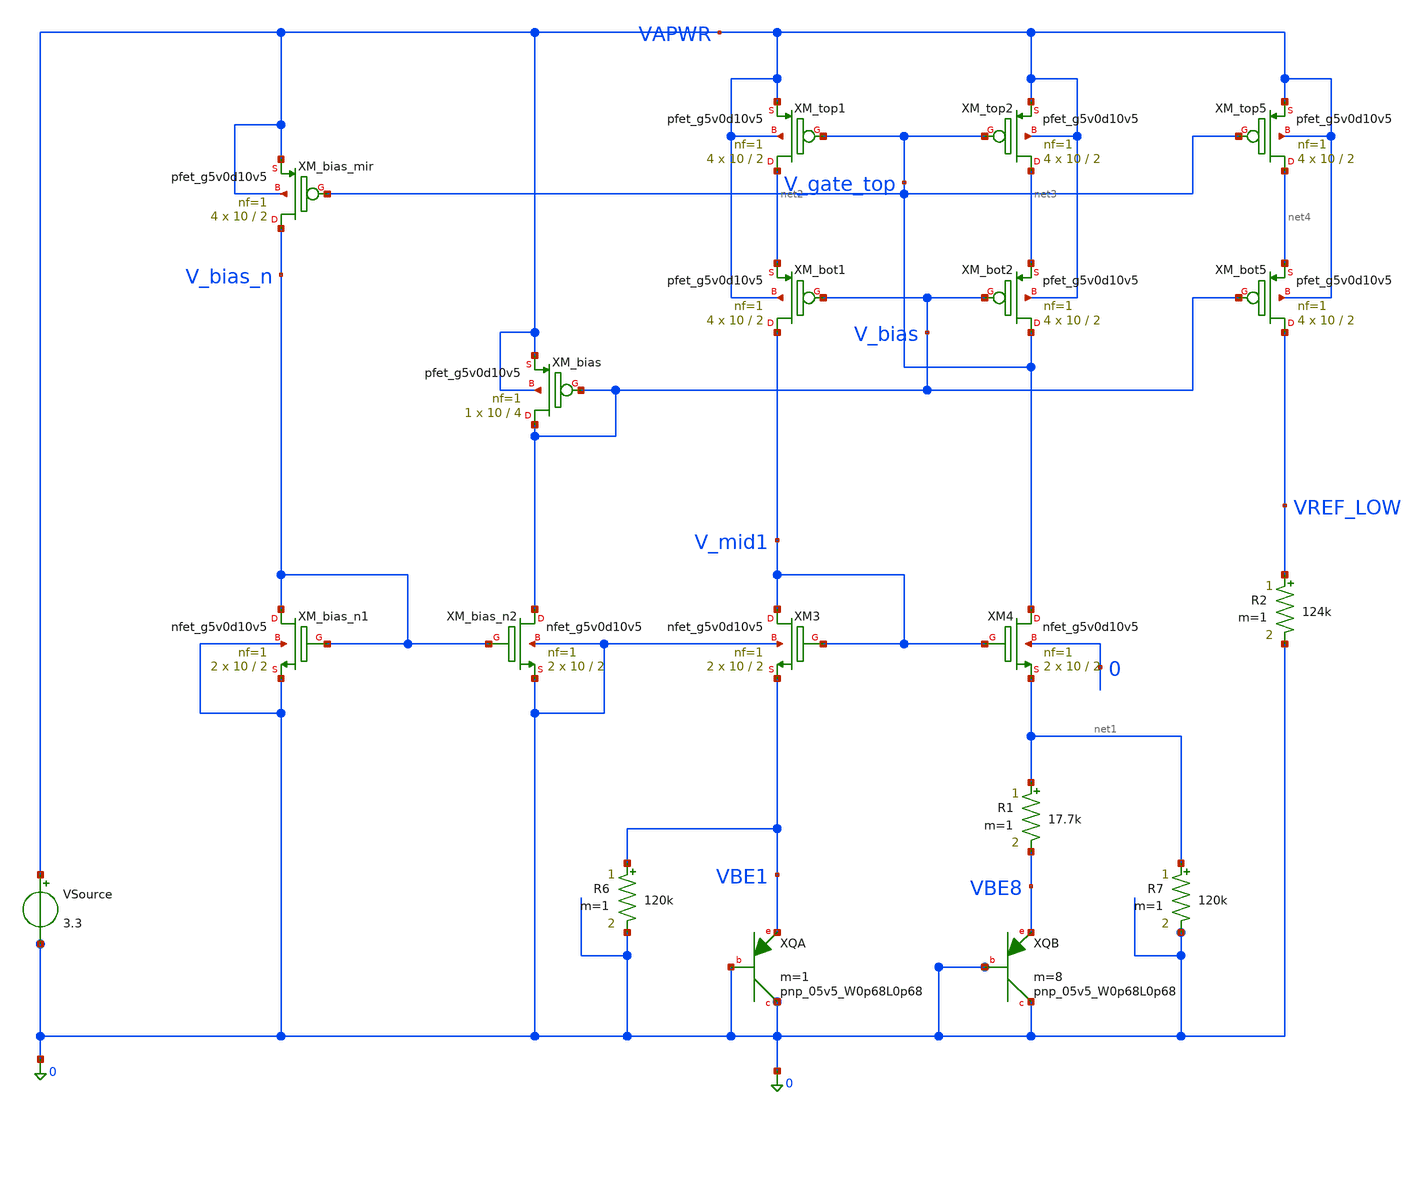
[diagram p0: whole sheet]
** sch_path: designs/bgr_ldo/milestones/05_selfbias_complete/bgr_core_tb.sch
**.subckt bgr_core_tb
XXQA 0 0 VBE1 sky130_fd_pr__pnp_05v5_W0p68L0p68 m=1
VSource VAPWR 0 3.3
XXQB 0 0 VBE8 sky130_fd_pr__pnp_05v5_W0p68L0p68 m=8
R1 net1 VBE8 17.7k m=1
R7 net1 0 120k m=1
R6 VBE1 0 120k m=1
XXM_top1 net2 V_gate_top VAPWR VAPWR sky130_fd_pr__pfet_g5v0d10v5 L=2 W=10 nf=1 ad='int((1 + 1)/2) * 10 / 1 * 0.29'
+ as='int((1 + 2)/2) * 10 / 1 * 0.29' pd='2*int((1 + 1)/2) * (10 / 1 + 0.29)' ps='2*int((1 + 2)/2) * (10 / 1 + 0.29)'
+ nrd='0.29 / 10 ' nrs='0.29 / 10 ' sa=0 sb=0 sd=0 mult=4 m=4
XXM_top2 net3 V_gate_top VAPWR VAPWR sky130_fd_pr__pfet_g5v0d10v5 L=2 W=10 nf=1 ad='int((1 + 1)/2) * 10 / 1 * 0.29'
+ as='int((1 + 2)/2) * 10 / 1 * 0.29' pd='2*int((1 + 1)/2) * (10 / 1 + 0.29)' ps='2*int((1 + 2)/2) * (10 / 1 + 0.29)'
+ nrd='0.29 / 10 ' nrs='0.29 / 10 ' sa=0 sb=0 sd=0 mult=4 m=4
XXM_top5 net4 V_gate_top VAPWR VAPWR sky130_fd_pr__pfet_g5v0d10v5 L=2 W=10 nf=1 ad='int((1 + 1)/2) * 10 / 1 * 0.29'
+ as='int((1 + 2)/2) * 10 / 1 * 0.29' pd='2*int((1 + 1)/2) * (10 / 1 + 0.29)' ps='2*int((1 + 2)/2) * (10 / 1 + 0.29)'
+ nrd='0.29 / 10 ' nrs='0.29 / 10 ' sa=0 sb=0 sd=0 mult=4 m=4
XXM3 V_mid1 V_mid1 VBE1 0 sky130_fd_pr__nfet_g5v0d10v5 L=2 W=10 nf=1 ad='int((1 + 1)/2) * 10 / 1 * 0.29'
+ as='int((1 + 2)/2) * 10 / 1 * 0.29' pd='2*int((1 + 1)/2) * (10 / 1 + 0.29)' ps='2*int((1 + 2)/2) * (10 / 1 + 0.29)'
+ nrd='0.29 / 10 ' nrs='0.29 / 10 ' sa=0 sb=0 sd=0 mult=2 m=2
XXM4 V_gate_top V_mid1 net1 0 sky130_fd_pr__nfet_g5v0d10v5 L=2 W=10 nf=1 ad='int((1 + 1)/2) * 10 / 1 * 0.29'
+ as='int((1 + 2)/2) * 10 / 1 * 0.29' pd='2*int((1 + 1)/2) * (10 / 1 + 0.29)' ps='2*int((1 + 2)/2) * (10 / 1 + 0.29)'
+ nrd='0.29 / 10 ' nrs='0.29 / 10 ' sa=0 sb=0 sd=0 mult=2 m=2
XXM_bot1 V_mid1 V_bias net2 VAPWR sky130_fd_pr__pfet_g5v0d10v5 L=2 W=10 nf=1 ad='int((1 + 1)/2) * 10 / 1 * 0.29'
+ as='int((1 + 2)/2) * 10 / 1 * 0.29' pd='2*int((1 + 1)/2) * (10 / 1 + 0.29)' ps='2*int((1 + 2)/2) * (10 / 1 + 0.29)'
+ nrd='0.29 / 10 ' nrs='0.29 / 10 ' sa=0 sb=0 sd=0 mult=4 m=4
XXM_bot2 V_gate_top V_bias net3 VAPWR sky130_fd_pr__pfet_g5v0d10v5 L=2 W=10 nf=1 ad='int((1 + 1)/2) * 10 / 1 * 0.29'
+ as='int((1 + 2)/2) * 10 / 1 * 0.29' pd='2*int((1 + 1)/2) * (10 / 1 + 0.29)' ps='2*int((1 + 2)/2) * (10 / 1 + 0.29)'
+ nrd='0.29 / 10 ' nrs='0.29 / 10 ' sa=0 sb=0 sd=0 mult=4 m=4
XXM_bot5 VREF_LOW V_bias net4 VAPWR sky130_fd_pr__pfet_g5v0d10v5 L=2 W=10 nf=1 ad='int((1 + 1)/2) * 10 / 1 * 0.29'
+ as='int((1 + 2)/2) * 10 / 1 * 0.29' pd='2*int((1 + 1)/2) * (10 / 1 + 0.29)' ps='2*int((1 + 2)/2) * (10 / 1 + 0.29)'
+ nrd='0.29 / 10 ' nrs='0.29 / 10 ' sa=0 sb=0 sd=0 mult=4 m=4
XXM_bias V_bias V_bias VAPWR VAPWR sky130_fd_pr__pfet_g5v0d10v5 L=4 W=10 nf=1 ad='int((1 + 1)/2) * 10 / 1 * 0.29'
+ as='int((1 + 2)/2) * 10 / 1 * 0.29' pd='2*int((1 + 1)/2) * (10 / 1 + 0.29)' ps='2*int((1 + 2)/2) * (10 / 1 + 0.29)'
+ nrd='0.29 / 10 ' nrs='0.29 / 10 ' sa=0 sb=0 sd=0 mult=1 m=1
R2 VREF_LOW 0 124k m=1
XXM_bias_mir V_bias_n V_gate_top VAPWR VAPWR sky130_fd_pr__pfet_g5v0d10v5 L=2 W=10 nf=1 ad='int((1 + 1)/2) * 10 / 1 * 0.29'
+ as='int((1 + 2)/2) * 10 / 1 * 0.29' pd='2*int((1 + 1)/2) * (10 / 1 + 0.29)' ps='2*int((1 + 2)/2) * (10 / 1 + 0.29)'
+ nrd='0.29 / 10 ' nrs='0.29 / 10 ' sa=0 sb=0 sd=0 mult=4 m=4
XXM_bias_n1 V_bias_n V_bias_n 0 0 sky130_fd_pr__nfet_g5v0d10v5 L=2 W=10 nf=1 ad='int((1 + 1)/2) * 10 / 1 * 0.29'
+ as='int((1 + 2)/2) * 10 / 1 * 0.29' pd='2*int((1 + 1)/2) * (10 / 1 + 0.29)' ps='2*int((1 + 2)/2) * (10 / 1 + 0.29)'
+ nrd='0.29 / 10 ' nrs='0.29 / 10 ' sa=0 sb=0 sd=0 mult=2 m=2
XXM_bias_n2 V_bias V_bias_n 0 0 sky130_fd_pr__nfet_g5v0d10v5 L=2 W=10 nf=1 ad='int((1 + 1)/2) * 10 / 1 * 0.29'
+ as='int((1 + 2)/2) * 10 / 1 * 0.29' pd='2*int((1 + 1)/2) * (10 / 1 + 0.29)' ps='2*int((1 + 2)/2) * (10 / 1 + 0.29)'
+ nrd='0.29 / 10 ' nrs='0.29 / 10 ' sa=0 sb=0 sd=0 mult=2 m=2
**** begin user architecture code

.nodeset v(vbe1)=0.78 v(net1)=0.78 v(v_mid1)=1.95 v(v_gate_top)=2.14 v(v_bias)=1.82 v(v_bias_n)=0.91
.save all
.dc temp -40 125 5

.control
  run
  write bgr_core_tb.raw
  plot v(vref_low)
  plot v(vbe1)-v(net1)
  echo =========================================================
  echo  BGR Core DC Operating Point (27 C)
  echo =========================================================
  print v(vref_low)
  print v(vbe1) v(net1) (v(vbe1)-v(net1))
  print v(v_mid1) v(v_gate_top) v(v_bias)
  print @m.xxm_top1.msky130_fd_pr__pfet_g5v0d10v5[id] @m.xxm_top2.msky130_fd_pr__pfet_g5v0d10v5[id]
+ @m.xxm_top5.msky130_fd_pr__pfet_g5v0d10v5[id]
.endc


** opencircuitdesign pdks install
.lib $::SKYWATER_MODELS/sky130.lib.spice tt

**** end user architecture code
**.ends
.end
